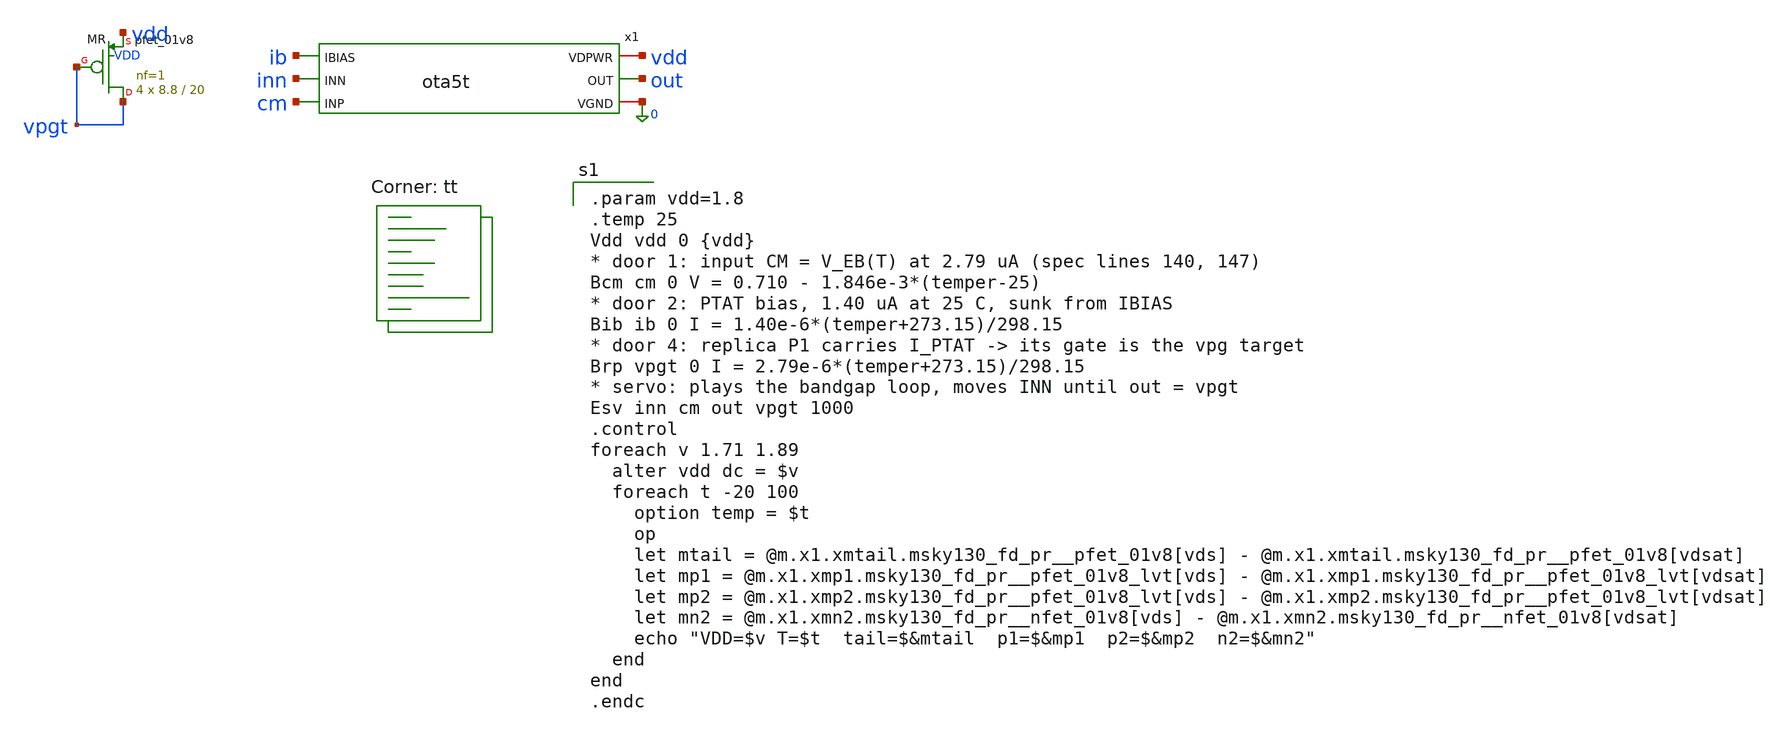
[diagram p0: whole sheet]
** sch_path: xschem/tb_ota5t_pvt.sch
**.subckt tb_ota5t_pvt
x1 vdd ib inn cm out 0 ota5t
XMR vpgt vpgt vdd VDD sky130_fd_pr__pfet_01v8 L=20 W=8.8 nf=1 ad='int((1 + 1)/2) * 8.8 / 1 * 0.29' as='int((1 + 2)/2) * 8.8 / 1 * 0.29'
+ pd='2*int((1 + 1)/2) * (8.8 / 1 + 0.29)' ps='2*int((1 + 2)/2) * (8.8 / 1 + 0.29)' nrd='0.29 / 8.8 ' nrs='0.29 / 8.8 '
+ sa=0 sb=0 sd=0 mult=4 m=4
**** begin user architecture code
.lib $::SKYWATER_MODELS/sky130.lib.spice tt

.param vdd=1.8
.temp 25
Vdd vdd 0 {vdd}
* door 1: input CM = V_EB(T) at 2.79 uA (spec lines 140, 147)
Bcm cm 0 V = 0.710 - 1.846e-3*(temper-25)
* door 2: PTAT bias, 1.40 uA at 25 C, sunk from IBIAS
Bib ib 0 I = 1.40e-6*(temper+273.15)/298.15
* door 4: replica P1 carries I_PTAT -> its gate is the vpg target
Brp vpgt 0 I = 2.79e-6*(temper+273.15)/298.15
* servo: plays the bandgap loop, moves INN until out = vpgt
Esv inn cm out vpgt 1000
.control
foreach v 1.71 1.89
  alter vdd dc = $v
  foreach t -20 100
    option temp = $t
    op
    let mtail = @m.x1.xmtail.msky130_fd_pr__pfet_01v8[vds] -
+ @m.x1.xmtail.msky130_fd_pr__pfet_01v8[vdsat]
    let mp1 = @m.x1.xmp1.msky130_fd_pr__pfet_01v8_lvt[vds] -
+ @m.x1.xmp1.msky130_fd_pr__pfet_01v8_lvt[vdsat]
    let mp2 = @m.x1.xmp2.msky130_fd_pr__pfet_01v8_lvt[vds] -
+ @m.x1.xmp2.msky130_fd_pr__pfet_01v8_lvt[vdsat]
    let mn2 = @m.x1.xmn2.msky130_fd_pr__nfet_01v8[vds] - @m.x1.xmn2.msky130_fd_pr__nfet_01v8[vdsat]
    echo "VDD=$v T=$t  tail=$&mtail  p1=$&mp1  p2=$&mp2  n2=$&mn2"
  end
end
.endc

**** end user architecture code
**.ends

* expanding   symbol:  ota5t.sym # of pins=6
** sym_path: xschem/ota5t.sym
** sch_path: xschem/ota5t.sch
.subckt ota5t VDPWR IBIAS INN INP OUT VGND
*.ipin INP
*.ipin INN
*.ipin IBIAS
*.opin OUT
*.iopin VDPWR
*.iopin VGND
XMREF IBIAS IBIAS VDPWR VDPWR sky130_fd_pr__pfet_01v8 L=4 W=20 nf=1 ad='int((1 + 1)/2) * 20 / 1 * 0.29'
+ as='int((1 + 2)/2) * 20 / 1 * 0.29' pd='2*int((1 + 1)/2) * (20 / 1 + 0.29)' ps='2*int((1 + 2)/2) * (20 / 1 + 0.29)'
+ nrd='0.29 / 20 ' nrs='0.29 / 20 ' sa=0 sb=0 sd=0 mult=1 m=1
XMTAIL tail IBIAS VDPWR VDPWR sky130_fd_pr__pfet_01v8 L=4 W=20 nf=1 ad='int((1 + 1)/2) * 20 / 1 * 0.29'
+ as='int((1 + 2)/2) * 20 / 1 * 0.29' pd='2*int((1 + 1)/2) * (20 / 1 + 0.29)' ps='2*int((1 + 2)/2) * (20 / 1 + 0.29)'
+ nrd='0.29 / 20 ' nrs='0.29 / 20 ' sa=0 sb=0 sd=0 mult=2 m=2
XMP1 dl INP tail VDPWR sky130_fd_pr__pfet_01v8_lvt L=6 W=25 nf=1 ad='int((1 + 1)/2) * 25 / 1 * 0.29'
+ as='int((1 + 2)/2) * 25 / 1 * 0.29' pd='2*int((1 + 1)/2) * (25 / 1 + 0.29)' ps='2*int((1 + 2)/2) * (25 / 1 + 0.29)'
+ nrd='0.29 / 25 ' nrs='0.29 / 25 ' sa=0 sb=0 sd=0 mult=24 m=24
XMP2 OUT INN tail VDPWR sky130_fd_pr__pfet_01v8_lvt L=6 W=25 nf=1 ad='int((1 + 1)/2) * 25 / 1 * 0.29'
+ as='int((1 + 2)/2) * 25 / 1 * 0.29' pd='2*int((1 + 1)/2) * (25 / 1 + 0.29)' ps='2*int((1 + 2)/2) * (25 / 1 + 0.29)'
+ nrd='0.29 / 25 ' nrs='0.29 / 25 ' sa=0 sb=0 sd=0 mult=24 m=24
XMN1 dl dl VGND VGND sky130_fd_pr__nfet_01v8 L=20 W=6 nf=1 ad='int((1 + 1)/2) * 6 / 1 * 0.29' as='int((1 + 2)/2) * 6 / 1 * 0.29'
+ pd='2*int((1 + 1)/2) * (6 / 1 + 0.29)' ps='2*int((1 + 2)/2) * (6 / 1 + 0.29)' nrd='0.29 / 6 ' nrs='0.29 / 6 '
+ sa=0 sb=0 sd=0 mult=2 m=2
XMN2 OUT dl VGND VGND sky130_fd_pr__nfet_01v8 L=20 W=6 nf=1 ad='int((1 + 1)/2) * 6 / 1 * 0.29' as='int((1 + 2)/2) * 6 / 1 * 0.29'
+ pd='2*int((1 + 1)/2) * (6 / 1 + 0.29)' ps='2*int((1 + 2)/2) * (6 / 1 + 0.29)' nrd='0.29 / 6 ' nrs='0.29 / 6 '
+ sa=0 sb=0 sd=0 mult=2 m=2
.ends

.end
